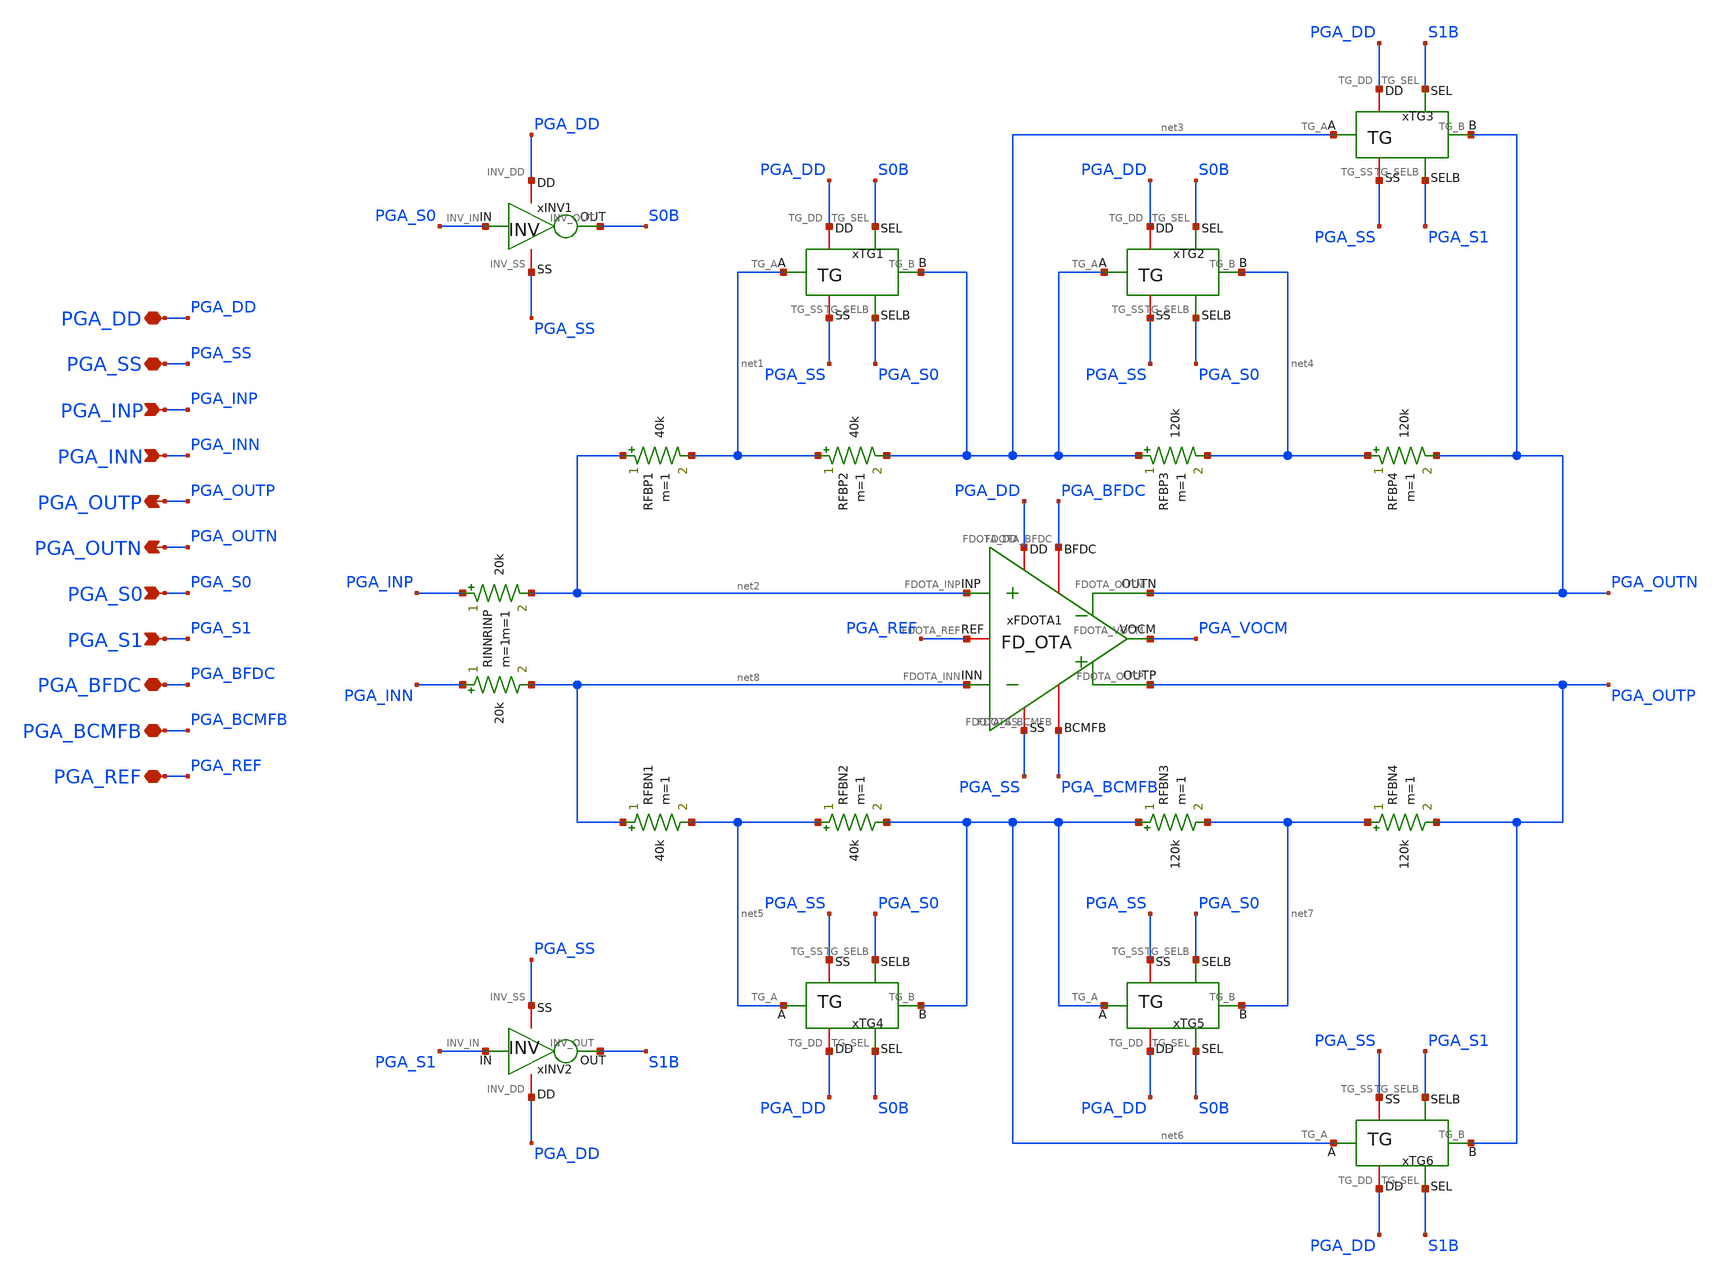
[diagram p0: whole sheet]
** sch_path: Design_Files/IC Design/Schematic/PGA/PGA.sch
**.subckt PGA PGA_DD PGA_SS PGA_INP PGA_INN PGA_OUTP PGA_BFDC PGA_OUTN PGA_BCMFB PGA_REF PGA_S0
*+ PGA_S1
*.iopin PGA_DD
*.iopin PGA_SS
*.ipin PGA_INP
*.ipin PGA_INN
*.opin PGA_OUTP
*.iopin PGA_BFDC
*.opin PGA_OUTN
*.iopin PGA_BCMFB
*.iopin PGA_REF
*.ipin PGA_S0
*.ipin PGA_S1
RFBP1 net2 net1 40k m=1
xFDOTA1 PGA_DD PGA_SS net2 net8 PGA_OUTN PGA_BFDC PGA_OUTP PGA_BCMFB PGA_REF PGA_VOCM FD_OTA
RFBP2 net1 net3 40k m=1
RFBP3 net3 net4 120k m=1
RFBP4 net4 PGA_OUTN 120k m=1
RINN PGA_INN net8 20k m=1
RINP PGA_INP net2 20k m=1
xTG1 PGA_DD PGA_SS net1 net3 S0B PGA_S0 TG
xTG3 PGA_DD PGA_SS net3 PGA_OUTN S1B PGA_S1 TG
xINV1 PGA_DD PGA_SS PGA_S0 S0B INV
xTG2 PGA_DD PGA_SS net3 net4 S0B PGA_S0 TG
RFBN1 net8 net5 40k m=1
RFBN2 net5 net6 40k m=1
RFBN3 net6 net7 120k m=1
RFBN4 net7 PGA_OUTP 120k m=1
xTG4 PGA_DD PGA_SS net5 net6 S0B PGA_S0 TG
xTG5 PGA_DD PGA_SS net6 net7 S0B PGA_S0 TG
xINV2 PGA_DD PGA_SS PGA_S1 S1B INV
xTG6 PGA_DD PGA_SS net6 PGA_OUTP S1B PGA_S1 TG
**.ends

* expanding   symbol:  ECG_Acquisition_IC/Design_Files/IC Design/Schematic/FD_OTA/FDOTA/FD_OTA.sym #
*+ of pins=10
** sym_path: Design_Files/IC Design/Schematic/FD_OTA/FDOTA/FD_OTA.sym
** sch_path: Design_Files/IC Design/Schematic/FD_OTA/FDOTA/FD_OTA.sch
.subckt FD_OTA FDOTA_DD FDOTA_SS FDOTA_INP FDOTA_INN FDOTA_OUTN FDOTA_BFDC FDOTA_OUTP FDOTA_BCMFB
+ FDOTA_REF FDOTA_VOCM
*.iopin FDOTA_DD
*.iopin FDOTA_SS
*.ipin FDOTA_INP
*.ipin FDOTA_INN
*.opin FDOTA_OUTP
*.iopin FDOTA_BFDC
*.opin FDOTA_OUTN
*.iopin FDOTA_BCMFB
*.iopin FDOTA_REF
*.iopin FDOTA_VOCM
R1 FDOTA_OUTP FDOTA_VOCM 100k m=1
R2 FDOTA_VOCM FDOTA_OUTN 100k m=1
C1 FDOTA_OUTP FDOTA_VOCM 50f m=1
C2 FDOTA_VOCM FDOTA_OUTN 50f m=1
xFDC1 FDOTA_DD FDOTA_SS FDOTA_INP FDOTA_INN FDOTA_OUTN FDOTA_BFDC FDOTA_OUTP FDOTA_VCMFB FDC
xCMFB1 FDOTA_DD FDOTA_SS FDOTA_VOCM FDOTA_REF FDOTA_VCMFB FDOTA_BCMFB CMFB
.ends


* expanding   symbol:  ECG_Acquisition_IC/Design_Files/IC Design/Schematic/TG/TG.sym # of pins=6
** sym_path: Design_Files/IC Design/Schematic/TG/TG.sym
** sch_path: Design_Files/IC Design/Schematic/TG/TG.sch
.subckt TG TG_DD TG_SS TG_A TG_B TG_SEL TG_SELB
*.iopin TG_DD
*.iopin TG_SS
*.iopin TG_A
*.iopin TG_B
*.ipin TG_SEL
*.ipin TG_SELB
XMTGP TG_B TG_SELB TG_A TG_DD pfet_03v3 L=0.5u W=10u nf=1 ad='int((nf+1)/2) * W/nf * 0.18u' as='int((nf+2)/2) * W/nf * 0.18u'
+ pd='2*int((nf+1)/2) * (W/nf + 0.18u)' ps='2*int((nf+2)/2) * (W/nf + 0.18u)' nrd='0.18u / W' nrs='0.18u / W'
+ sa=0 sb=0 sd=0 m=1
XMTGN TG_A TG_SEL TG_B TG_SS nfet_03v3 L=0.5u W=5u nf=1 ad='int((nf+1)/2) * W/nf * 0.18u' as='int((nf+2)/2) * W/nf * 0.18u'
+ pd='2*int((nf+1)/2) * (W/nf + 0.18u)' ps='2*int((nf+2)/2) * (W/nf + 0.18u)' nrd='0.18u / W' nrs='0.18u / W'
+ sa=0 sb=0 sd=0 m=1
.ends


* expanding   symbol:  ECG_Acquisition_IC/Design_Files/IC Design/Schematic/INV/INV.sym # of pins=4
** sym_path: Design_Files/IC Design/Schematic/INV/INV.sym
** sch_path: Design_Files/IC Design/Schematic/INV/INV.sch
.subckt INV INV_DD INV_SS INV_IN INV_OUT
*.iopin INV_DD
*.iopin INV_SS
*.ipin INV_IN
*.opin INV_OUT
XMINVP INV_OUT INV_IN INV_DD INV_DD pfet_03v3 L=0.5u W=2u nf=1 ad='int((nf+1)/2) * W/nf * 0.18u' as='int((nf+2)/2) * W/nf * 0.18u'
+ pd='2*int((nf+1)/2) * (W/nf + 0.18u)' ps='2*int((nf+2)/2) * (W/nf + 0.18u)' nrd='0.18u / W' nrs='0.18u / W'
+ sa=0 sb=0 sd=0 m=1
XMINVN INV_OUT INV_IN INV_SS INV_SS nfet_03v3 L=0.5u W=1u nf=1 ad='int((nf+1)/2) * W/nf * 0.18u' as='int((nf+2)/2) * W/nf * 0.18u'
+ pd='2*int((nf+1)/2) * (W/nf + 0.18u)' ps='2*int((nf+2)/2) * (W/nf + 0.18u)' nrd='0.18u / W' nrs='0.18u / W'
+ sa=0 sb=0 sd=0 m=1
.ends


* expanding   symbol:  ECG_Acquisition_IC/Design_Files/IC Design/Schematic/FD_OTA/FDC/FDC.sym # of
*+ pins=8
** sym_path: Design_Files/IC Design/Schematic/FD_OTA/FDC/FDC.sym
** sch_path: Design_Files/IC Design/Schematic/FD_OTA/FDC/FDC.sch
.subckt FDC FDC_DD FDC_SS FDC_INP FDC_INN FDC_OUTN FDC_B FDC_OUTP FDC_CMFB
*.iopin FDC_DD
*.iopin FDC_SS
*.ipin FDC_INP
*.ipin FDC_INN
*.opin FDC_OUTP
*.iopin FDC_B
*.opin FDC_OUTN
*.iopin FDC_CMFB
XM3 net4 FDC_CMFB FDC_DD FDC_DD pfet_03v3 L=2u W=1u nf=1 ad='int((nf+1)/2) * W/nf * 0.18u' as='int((nf+2)/2) * W/nf * 0.18u'
+ pd='2*int((nf+1)/2) * (W/nf + 0.18u)' ps='2*int((nf+2)/2) * (W/nf + 0.18u)' nrd='0.18u / W' nrs='0.18u / W'
+ sa=0 sb=0 sd=0 m=200
XM8 FDC_OUTP FDC_B FDC_SS FDC_SS nfet_03v3 L=0.5u W=1u nf=1 ad='int((nf+1)/2) * W/nf * 0.18u' as='int((nf+2)/2) * W/nf * 0.18u'
+ pd='2*int((nf+1)/2) * (W/nf + 0.18u)' ps='2*int((nf+2)/2) * (W/nf + 0.18u)' nrd='0.18u / W' nrs='0.18u / W'
+ sa=0 sb=0 sd=0 m=100
Rz net1 net2 3.5k m=1
XM5 net3 FDC_B FDC_SS FDC_SS nfet_03v3 L=2u W=1u nf=1 ad='int((nf+1)/2) * W/nf * 0.18u' as='int((nf+2)/2) * W/nf * 0.18u'
+ pd='2*int((nf+1)/2) * (W/nf + 0.18u)' ps='2*int((nf+2)/2) * (W/nf + 0.18u)' nrd='0.18u / W' nrs='0.18u / W'
+ sa=0 sb=0 sd=0 m=10
XM6 FDC_OUTP net1 FDC_DD FDC_DD pfet_03v3 L=0.5u W=1u nf=1 ad='int((nf+1)/2) * W/nf * 0.18u' as='int((nf+2)/2) * W/nf * 0.18u'
+ pd='2*int((nf+1)/2) * (W/nf + 0.18u)' ps='2*int((nf+2)/2) * (W/nf + 0.18u)' nrd='0.18u / W' nrs='0.18u / W'
+ sa=0 sb=0 sd=0 m=200
XM10 FDC_B FDC_B FDC_SS FDC_SS nfet_03v3 L=2u W=1u nf=1 ad='int((nf+1)/2) * W/nf * 0.18u' as='int((nf+2)/2) * W/nf * 0.18u'
+ pd='2*int((nf+1)/2) * (W/nf + 0.18u)' ps='2*int((nf+2)/2) * (W/nf + 0.18u)' nrd='0.18u / W' nrs='0.18u / W'
+ sa=0 sb=0 sd=0 m=20
Cc net2 FDC_OUTP 2.5p m=1
XM9 FDC_OUTN FDC_B FDC_SS FDC_SS nfet_03v3 L=0.5u W=1u nf=1 ad='int((nf+1)/2) * W/nf * 0.18u' as='int((nf+2)/2) * W/nf * 0.18u'
+ pd='2*int((nf+1)/2) * (W/nf + 0.18u)' ps='2*int((nf+2)/2) * (W/nf + 0.18u)' nrd='0.18u / W' nrs='0.18u / W'
+ sa=0 sb=0 sd=0 m=100
Rz1 net4 net5 3.5k m=1
XM7 FDC_OUTN net4 FDC_DD FDC_DD pfet_03v3 L=0.5u W=1u nf=1 ad='int((nf+1)/2) * W/nf * 0.18u' as='int((nf+2)/2) * W/nf * 0.18u'
+ pd='2*int((nf+1)/2) * (W/nf + 0.18u)' ps='2*int((nf+2)/2) * (W/nf + 0.18u)' nrd='0.18u / W' nrs='0.18u / W'
+ sa=0 sb=0 sd=0 m=200
Cc1 net5 FDC_OUTN 2.5p m=1
XM4 net1 FDC_CMFB FDC_DD FDC_DD pfet_03v3 L=2u W=1u nf=1 ad='int((nf+1)/2) * W/nf * 0.18u' as='int((nf+2)/2) * W/nf * 0.18u'
+ pd='2*int((nf+1)/2) * (W/nf + 0.18u)' ps='2*int((nf+2)/2) * (W/nf + 0.18u)' nrd='0.18u / W' nrs='0.18u / W'
+ sa=0 sb=0 sd=0 m=200
XM1 net4 FDC_INN net3 FDC_SS nfet_03v3 L=2u W=1u nf=1 ad='int((nf+1)/2) * W/nf * 0.18u' as='int((nf+2)/2) * W/nf * 0.18u'
+ pd='2*int((nf+1)/2) * (W/nf + 0.18u)' ps='2*int((nf+2)/2) * (W/nf + 0.18u)' nrd='0.18u / W' nrs='0.18u / W'
+ sa=0 sb=0 sd=0 m=200
XM2 net1 FDC_INP net3 FDC_SS nfet_03v3 L=2u W=1u nf=1 ad='int((nf+1)/2) * W/nf * 0.18u' as='int((nf+2)/2) * W/nf * 0.18u'
+ pd='2*int((nf+1)/2) * (W/nf + 0.18u)' ps='2*int((nf+2)/2) * (W/nf + 0.18u)' nrd='0.18u / W' nrs='0.18u / W'
+ sa=0 sb=0 sd=0 m=200
.ends


* expanding   symbol:  ECG_Acquisition_IC/Design_Files/IC Design/Schematic/FD_OTA/CMFB/CMFB.sym # of
*+ pins=6
** sym_path: Design_Files/IC Design/Schematic/FD_OTA/CMFB/CMFB.sym
** sch_path: Design_Files/IC Design/Schematic/FD_OTA/CMFB/CMFB.sch
.subckt CMFB CMFB_DD CMFB_SS CMFB_IN CMFB_REF CMFB_OUT CMFB_B
*.iopin CMFB_DD
*.iopin CMFB_SS
*.ipin CMFB_IN
*.ipin CMFB_REF
*.opin CMFB_OUT
*.iopin CMFB_B
XM4 CMFB_OUT CMFB_OUT CMFB_DD CMFB_DD pfet_03v3 L=0.5u W=1u nf=1 ad='int((nf+1)/2) * W/nf * 0.18u' as='int((nf+2)/2) * W/nf * 0.18u'
+ pd='2*int((nf+1)/2) * (W/nf + 0.18u)' ps='2*int((nf+2)/2) * (W/nf + 0.18u)' nrd='0.18u / W' nrs='0.18u / W'
+ sa=0 sb=0 sd=0 m=77
XM3 net2 net2 CMFB_DD CMFB_DD pfet_03v3 L=0.5u W=1u nf=1 ad='int((nf+1)/2) * W/nf * 0.18u' as='int((nf+2)/2) * W/nf * 0.18u'
+ pd='2*int((nf+1)/2) * (W/nf + 0.18u)' ps='2*int((nf+2)/2) * (W/nf + 0.18u)' nrd='0.18u / W' nrs='0.18u / W'
+ sa=0 sb=0 sd=0 m=77
XM1 net2 CMFB_REF net1 CMFB_SS nfet_03v3 L=0.5u W=1u nf=1 ad='int((nf+1)/2) * W/nf * 0.18u' as='int((nf+2)/2) * W/nf * 0.18u'
+ pd='2*int((nf+1)/2) * (W/nf + 0.18u)' ps='2*int((nf+2)/2) * (W/nf + 0.18u)' nrd='0.18u / W' nrs='0.18u / W'
+ sa=0 sb=0 sd=0 m=5
XM2 CMFB_OUT CMFB_IN net1 CMFB_SS nfet_03v3 L=0.5u W=1u nf=1 ad='int((nf+1)/2) * W/nf * 0.18u' as='int((nf+2)/2) * W/nf * 0.18u'
+ pd='2*int((nf+1)/2) * (W/nf + 0.18u)' ps='2*int((nf+2)/2) * (W/nf + 0.18u)' nrd='0.18u / W' nrs='0.18u / W'
+ sa=0 sb=0 sd=0 m=5
XM5 net1 CMFB_B CMFB_SS CMFB_SS nfet_03v3 L=2u W=1u nf=1 ad='int((nf+1)/2) * W/nf * 0.18u' as='int((nf+2)/2) * W/nf * 0.18u'
+ pd='2*int((nf+1)/2) * (W/nf + 0.18u)' ps='2*int((nf+2)/2) * (W/nf + 0.18u)' nrd='0.18u / W' nrs='0.18u / W'
+ sa=0 sb=0 sd=0 m=20
XM10 CMFB_B CMFB_B CMFB_SS CMFB_SS nfet_03v3 L=2u W=1u nf=1 ad='int((nf+1)/2) * W/nf * 0.18u' as='int((nf+2)/2) * W/nf * 0.18u'
+ pd='2*int((nf+1)/2) * (W/nf + 0.18u)' ps='2*int((nf+2)/2) * (W/nf + 0.18u)' nrd='0.18u / W' nrs='0.18u / W'
+ sa=0 sb=0 sd=0 m=20
.ends

.end
